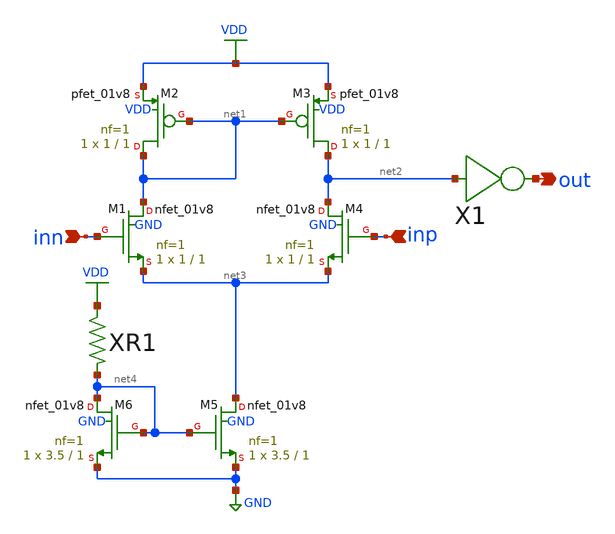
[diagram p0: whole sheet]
** sch_path: xschem/comp.sch
**.subckt comp inp inn out
*.ipin inp
*.ipin inn
*.opin out
XM1 net1 inn net3 GND sky130_fd_pr__nfet_01v8 L=1 W=1 nf=1 ad='int((1 + 1)/2) * 1 / 1 * 0.29' as='int((1 + 2)/2) * 1 / 1 * 0.29'
+ pd='2*int((1 + 1)/2) * (1 / 1 + 0.29)' ps='2*int((1 + 2)/2) * (1 / 1 + 0.29)' nrd='0.29 / 1 ' nrs='0.29 / 1 '
+ sa=0 sb=0 sd=0 mult=1 m=1
XM2 net1 net1 VDD VDD sky130_fd_pr__pfet_01v8 L=1 W=1 nf=1 ad='int((1 + 1)/2) * 1 / 1 * 0.29' as='int((1 + 2)/2) * 1 / 1 * 0.29'
+ pd='2*int((1 + 1)/2) * (1 / 1 + 0.29)' ps='2*int((1 + 2)/2) * (1 / 1 + 0.29)' nrd='0.29 / 1 ' nrs='0.29 / 1 '
+ sa=0 sb=0 sd=0 mult=1 m=1
XM3 net2 net1 VDD VDD sky130_fd_pr__pfet_01v8 L=1 W=1 nf=1 ad='int((1 + 1)/2) * 1 / 1 * 0.29' as='int((1 + 2)/2) * 1 / 1 * 0.29'
+ pd='2*int((1 + 1)/2) * (1 / 1 + 0.29)' ps='2*int((1 + 2)/2) * (1 / 1 + 0.29)' nrd='0.29 / 1 ' nrs='0.29 / 1 '
+ sa=0 sb=0 sd=0 mult=1 m=1
XM4 net2 inp net3 GND sky130_fd_pr__nfet_01v8 L=1 W=1 nf=1 ad='int((1 + 1)/2) * 1 / 1 * 0.29' as='int((1 + 2)/2) * 1 / 1 * 0.29'
+ pd='2*int((1 + 1)/2) * (1 / 1 + 0.29)' ps='2*int((1 + 2)/2) * (1 / 1 + 0.29)' nrd='0.29 / 1 ' nrs='0.29 / 1 '
+ sa=0 sb=0 sd=0 mult=1 m=1
XM5 net3 net4 GND GND sky130_fd_pr__nfet_01v8 L=1 W=3.5 nf=1 ad='int((1 + 1)/2) * 3.5 / 1 * 0.29' as='int((1 + 2)/2) * 3.5 / 1 * 0.29'
+ pd='2*int((1 + 1)/2) * (3.5 / 1 + 0.29)' ps='2*int((1 + 2)/2) * (3.5 / 1 + 0.29)' nrd='0.29 / 3.5 ' nrs='0.29 / 3.5 '
+ sa=0 sb=0 sd=0 mult=1 m=1
XM6 net4 net4 GND GND sky130_fd_pr__nfet_01v8 L=1 W=3.5 nf=1 ad='int((1 + 1)/2) * 3.5 / 1 * 0.29' as='int((1 + 2)/2) * 3.5 / 1 * 0.29'
+ pd='2*int((1 + 1)/2) * (3.5 / 1 + 0.29)' ps='2*int((1 + 2)/2) * (3.5 / 1 + 0.29)' nrd='0.29 / 3.5 ' nrs='0.29 / 3.5 '
+ sa=0 sb=0 sd=0 mult=1 m=1
XR1 net4 VDD res100k
X1 net2 out inverter
**.ends

* expanding   symbol:  res100k.sym # of pins=2
** sym_path: xschem/res100k.sym
** sch_path: xschem/res100k.sch
.subckt res100k bot top
*.iopin top
*.iopin bot
XR1 net1 top GND sky130_fd_pr__res_xhigh_po_0p35 L=3.5 mult=1 m=1
XR2 net2 net1 GND sky130_fd_pr__res_xhigh_po_0p35 L=3.5 mult=1 m=1
XR3 net3 net2 GND sky130_fd_pr__res_xhigh_po_0p35 L=3.5 mult=1 m=1
XR4 net4 net3 GND sky130_fd_pr__res_xhigh_po_0p35 L=3.5 mult=1 m=1
XR5 bot net4 GND sky130_fd_pr__res_xhigh_po_0p35 L=3.5 mult=1 m=1
.ends


* expanding   symbol:  inverter.sym # of pins=2
** sym_path: xschem/inverter.sym
** sch_path: xschem/inverter.sch
.subckt inverter a y
*.ipin a
*.opin y
XM1 y a GND GND sky130_fd_pr__nfet_01v8 L=0.15 W=1 nf=1 ad='int((1 + 1)/2) * 1 / 1 * 0.29' as='int((1 + 2)/2) * 1 / 1 * 0.29'
+ pd='2*int((1 + 1)/2) * (1 / 1 + 0.29)' ps='2*int((1 + 2)/2) * (1 / 1 + 0.29)' nrd='0.29 / 1 ' nrs='0.29 / 1 '
+ sa=0 sb=0 sd=0 mult=1 m=1
XM2 y a VDD VDD sky130_fd_pr__pfet_01v8 L=0.15 W=1 nf=1 ad='int((1 + 1)/2) * 1 / 1 * 0.29' as='int((1 + 2)/2) * 1 / 1 * 0.29'
+ pd='2*int((1 + 1)/2) * (1 / 1 + 0.29)' ps='2*int((1 + 2)/2) * (1 / 1 + 0.29)' nrd='0.29 / 1 ' nrs='0.29 / 1 '
+ sa=0 sb=0 sd=0 mult=1 m=1
.ends

.GLOBAL VDD
.GLOBAL GND
.end
